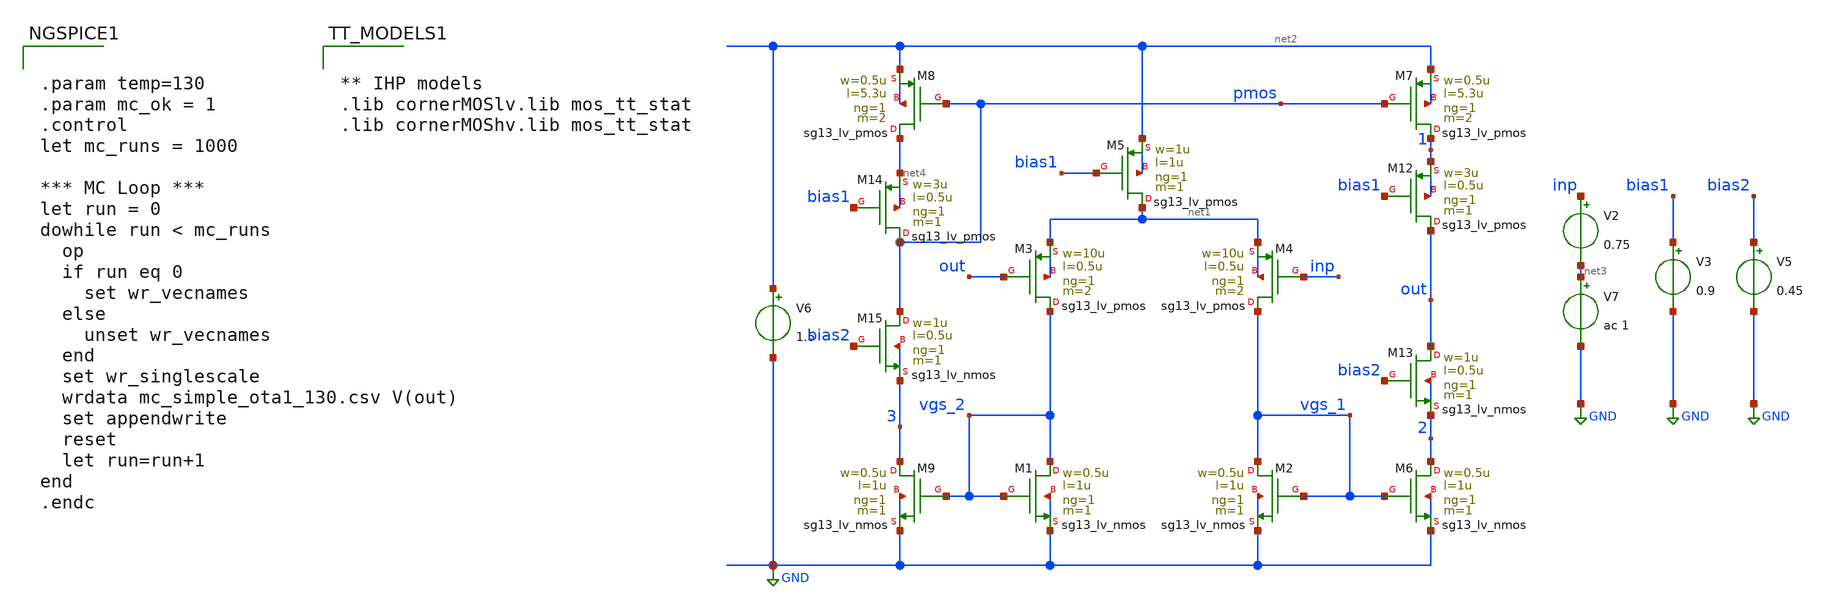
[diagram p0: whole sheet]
** sch_path: 10_xschem/ota_testbench_mc.sch
**.subckt ota_testbench_mc
XM1 vgs_2 vgs_2 GND GND sg13_lv_nmos w=0.5u l=1u ng=1 m=1 mm_ok=1
XM3 vgs_2 out net1 net1 sg13_lv_pmos w=10u l=0.5u ng=1 m=2 mm_ok=1
XM4 vgs_1 inp net1 net1 sg13_lv_pmos w=10u l=0.5u ng=1 m=2 mm_ok=1
XM2 vgs_1 vgs_1 GND GND sg13_lv_nmos w=0.5u l=1u ng=1 m=1 mm_ok=1
XM5 net1 bias1 net2 net2 sg13_lv_pmos w=1u l=1u ng=1 m=1 mm_ok=1
XM6 2 vgs_1 GND GND sg13_lv_nmos w=0.5u l=1u ng=1 m=1 mm_ok=1
XM7 1 pmos net2 net2 sg13_lv_pmos w=0.5u l=5.3u ng=1 m=2 mm_ok=1
XM8 net4 pmos net2 net2 sg13_lv_pmos w=0.5u l=5.3u ng=1 m=2 mm_ok=1
XM9 3 vgs_2 GND GND sg13_lv_nmos w=0.5u l=1u ng=1 m=1 mm_ok=1
V3 bias1 GND 0.9
V2 inp net3 0.75
V6 net2 GND 1.5
V7 net3 GND ac 1
XM12 out bias1 1 1 sg13_lv_pmos w=3u l=0.5u ng=1 m=1 mm_ok=1
XM13 out bias2 2 2 sg13_lv_nmos w=1u l=0.5u ng=1 m=1 mm_ok=1
XM14 pmos bias1 net4 net4 sg13_lv_pmos w=3u l=0.5u ng=1 m=1 mm_ok=1
XM15 pmos bias2 3 3 sg13_lv_nmos w=1u l=0.5u ng=1 m=1 mm_ok=1
V5 bias2 GND 0.45
**** begin user architecture code


** IHP models
.lib cornerMOSlv.lib mos_tt_stat
.lib cornerMOShv.lib mos_tt_stat




.param temp=130
.param mc_ok = 1
.control
let mc_runs = 1000

*** MC Loop ***
let run = 0
dowhile run < mc_runs
  op
  if run eq 0
    set wr_vecnames
  else
    unset wr_vecnames
  end
  set wr_singlescale
  wrdata mc_simple_ota1_130.csv V(out)
  set appendwrite
  reset
  let run=run+1
end
.endc


**** end user architecture code
**.ends
.GLOBAL GND
.end
